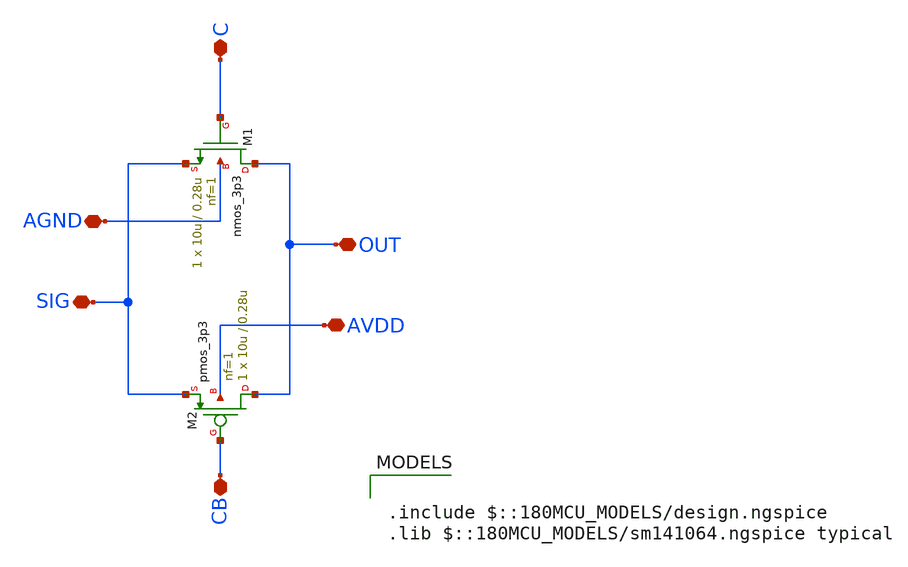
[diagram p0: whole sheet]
** sch_path: Designs/tg.sch
**.subckt tg CB OUT AVDD AGND SIG C
*.iopin CB
*.iopin OUT
*.iopin AVDD
*.iopin AGND
*.iopin SIG
*.iopin C
XM1 OUT C SIG AGND nmos_3p3 L=0.28u W=10u nf=1 ad='int((nf+1)/2) * W/nf * 0.18u' as='int((nf+2)/2) * W/nf * 0.18u'
+ pd='2*int((nf+1)/2) * (W/nf + 0.18u)' ps='2*int((nf+2)/2) * (W/nf + 0.18u)' nrd='0.18u / W' nrs='0.18u / W'
+ sa=0 sb=0 sd=0 m=1
XM2 OUT CB SIG AVDD pmos_3p3 L=0.28u W=10u nf=1 ad='int((nf+1)/2) * W/nf * 0.18u' as='int((nf+2)/2) * W/nf * 0.18u'
+ pd='2*int((nf+1)/2) * (W/nf + 0.18u)' ps='2*int((nf+2)/2) * (W/nf + 0.18u)' nrd='0.18u / W' nrs='0.18u / W'
+ sa=0 sb=0 sd=0 m=1
**** begin user architecture code

.include $::180MCU_MODELS/design.ngspice
.lib $::180MCU_MODELS/sm141064.ngspice typical

**** end user architecture code
**.ends
.end
